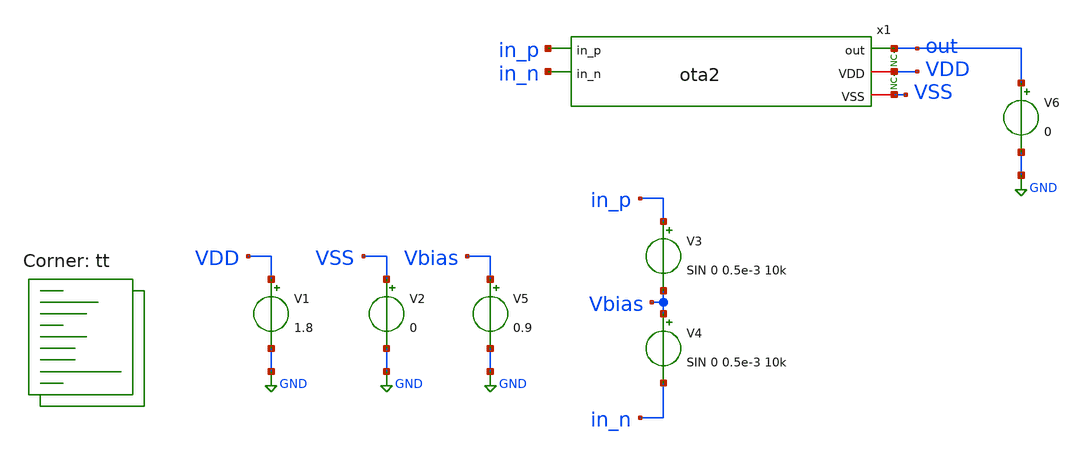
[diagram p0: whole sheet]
** sch_path: xschem/tests/ota2/ota2_test.sch
**.subckt ota2_test
V1 VDD GND 1.8
V2 VSS GND 0
V3 in_p Vbias SIN 0 0.5e-3 10k
V4 Vbias in_n SIN 0 0.5e-3 10k
V5 Vbias GND 0.9
* noconn VDD
* noconn out
x1 out in_p in_n VDD VSS ota2
V6 out GND 0
**** begin user architecture code
.lib $::SKYWATER_MODELS/sky130.lib.spice tt
 *.lib $::SKYWATER_MODELS/sky130.lib.spice tt
.include $::SKYWATER_STDCELLS/sky130_fd_sc_hd.spice




* ngspice commands
* ngspice commands
.options list act
.options method=gear
.temp 25

.control
save all
tran 1u 300u
plot in_p-in_n
plot diff_out
plot in_p-in_n+0.9 out
plot out
meas tran outptp pp v(out) from=0s to=300us
meas tran outmean avg v(out) from=0s to=300us

let gain = 20*log10($&outptp/0.002)
echo gain = $&gain

write ota2_test.raw
.endc



**** end user architecture code
**.ends
.GLOBAL GND
.end
